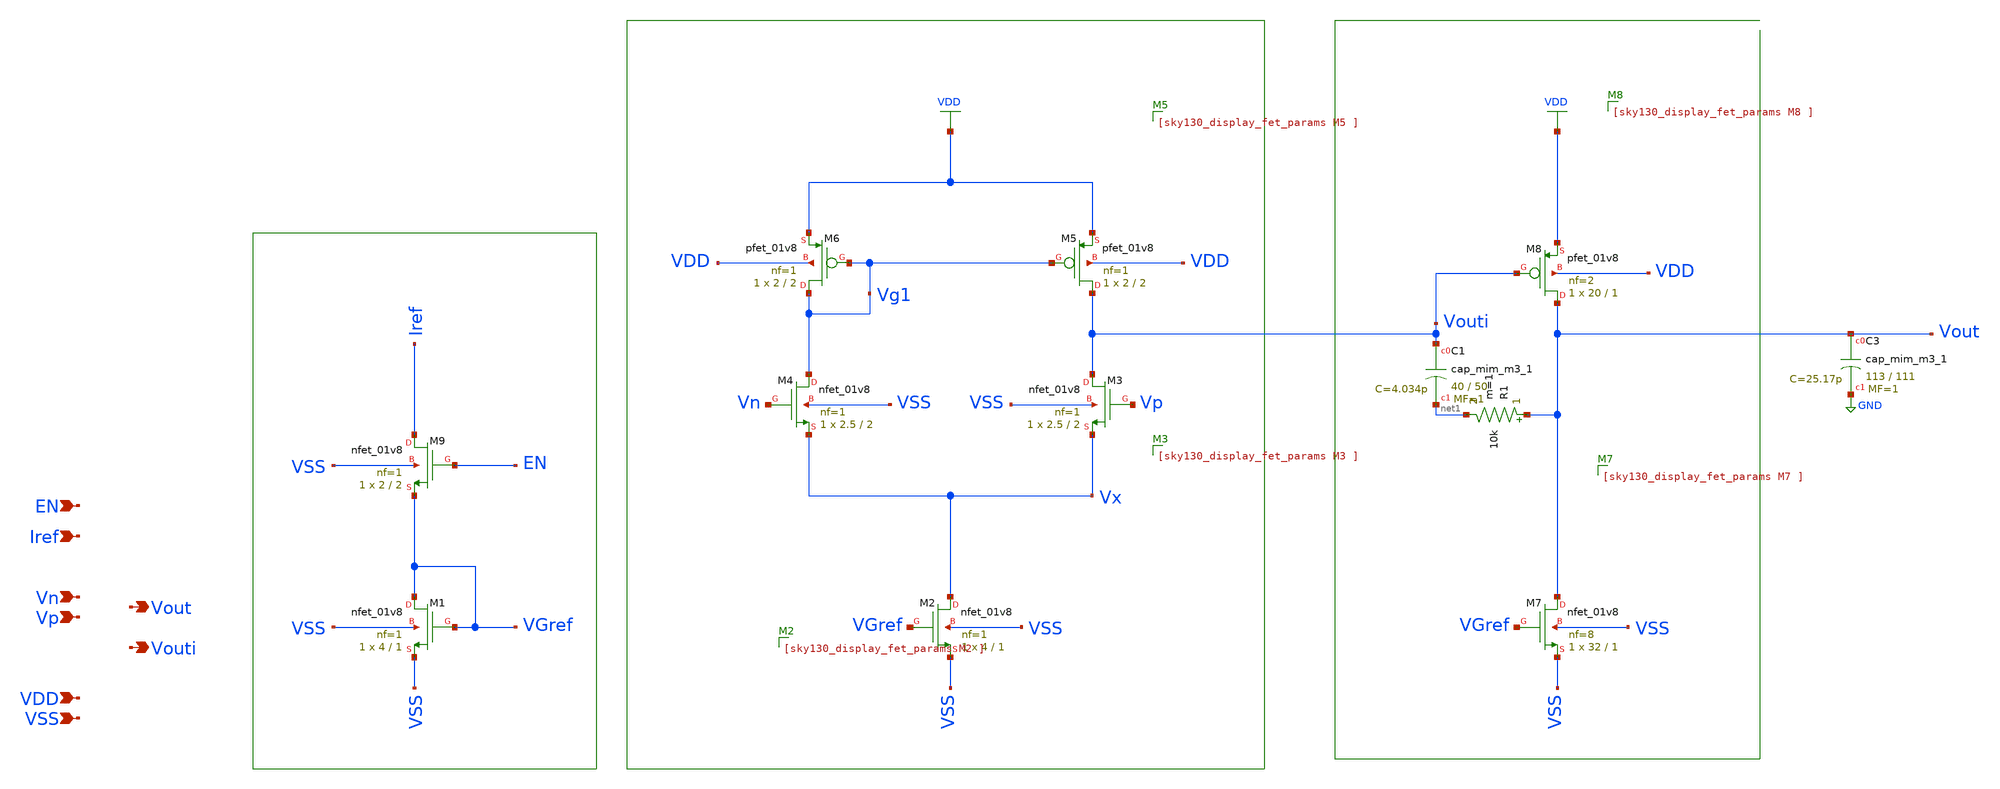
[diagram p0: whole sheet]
** sch_path: xschem/opamp.sch
**.subckt opamp VSS Vp Vout Vn VDD Iref Vouti EN
*.ipin VSS
*.ipin Vp
*.opin Vout
*.ipin Vn
*.ipin VDD
*.ipin Iref
*.opin Vouti
*.ipin EN
XM1 VGref VGref VSS VSS sky130_fd_pr__nfet_01v8 L=1 W=4 nf=1 ad='int((1 + 1)/2) * 4 / 1 * 0.29' as='int((1 + 2)/2) * 4 / 1 * 0.29'
+ pd='2*int((1 + 1)/2) * (4 / 1 + 0.29)' ps='2*int((1 + 2)/2) * (4 / 1 + 0.29)' nrd='0.29 / 4 ' nrs='0.29 / 4 '
+ sa=0 sb=0 sd=0 mult=1 m=1
XM2 Vx VGref VSS VSS sky130_fd_pr__nfet_01v8 L=1 W=4 nf=1 ad='int((1 + 1)/2) * 4 / 1 * 0.29' as='int((1 + 2)/2) * 4 / 1 * 0.29'
+ pd='2*int((1 + 1)/2) * (4 / 1 + 0.29)' ps='2*int((1 + 2)/2) * (4 / 1 + 0.29)' nrd='0.29 / 4 ' nrs='0.29 / 4 '
+ sa=0 sb=0 sd=0 mult=1 m=1
XM3 Vouti Vp Vx VSS sky130_fd_pr__nfet_01v8 L=2 W=2.5 nf=1 ad='int((1 + 1)/2) * 2.5 / 1 * 0.29' as='int((1 + 2)/2) * 2.5 / 1 * 0.29'
+ pd='2*int((1 + 1)/2) * (2.5 / 1 + 0.29)' ps='2*int((1 + 2)/2) * (2.5 / 1 + 0.29)' nrd='0.29 / 2.5 ' nrs='0.29 / 2.5 '
+ sa=0 sb=0 sd=0 mult=1 m=1
XM4 Vg1 Vn Vx VSS sky130_fd_pr__nfet_01v8 L=2 W=2.5 nf=1 ad='int((1 + 1)/2) * 2.5 / 1 * 0.29' as='int((1 + 2)/2) * 2.5 / 1 * 0.29'
+ pd='2*int((1 + 1)/2) * (2.5 / 1 + 0.29)' ps='2*int((1 + 2)/2) * (2.5 / 1 + 0.29)' nrd='0.29 / 2.5 ' nrs='0.29 / 2.5 '
+ sa=0 sb=0 sd=0 mult=1 m=1
XM5 Vouti Vg1 VDD VDD sky130_fd_pr__pfet_01v8 L=2 W=2 nf=1 ad='int((1 + 1)/2) * 2 / 1 * 0.29' as='int((1 + 2)/2) * 2 / 1 * 0.29'
+ pd='2*int((1 + 1)/2) * (2 / 1 + 0.29)' ps='2*int((1 + 2)/2) * (2 / 1 + 0.29)' nrd='0.29 / 2 ' nrs='0.29 / 2 '
+ sa=0 sb=0 sd=0 mult=1 m=1
XM6 Vg1 Vg1 VDD VDD sky130_fd_pr__pfet_01v8 L=2 W=2 nf=1 ad='int((1 + 1)/2) * 2 / 1 * 0.29' as='int((1 + 2)/2) * 2 / 1 * 0.29'
+ pd='2*int((1 + 1)/2) * (2 / 1 + 0.29)' ps='2*int((1 + 2)/2) * (2 / 1 + 0.29)' nrd='0.29 / 2 ' nrs='0.29 / 2 '
+ sa=0 sb=0 sd=0 mult=1 m=1
XM7 Vout VGref VSS VSS sky130_fd_pr__nfet_01v8 L=1 W=32 nf=8 ad='int((8 + 1)/2) * 32 / 8 * 0.29' as='int((8 + 2)/2) * 32 / 8 * 0.29'
+ pd='2*int((8 + 1)/2) * (32 / 8 + 0.29)' ps='2*int((8 + 2)/2) * (32 / 8 + 0.29)' nrd='0.29 / 32 ' nrs='0.29 / 32 '
+ sa=0 sb=0 sd=0 mult=1 m=1
XM8 Vout Vouti VDD VDD sky130_fd_pr__pfet_01v8 L=1 W=20 nf=2 ad='int((2 + 1)/2) * 20 / 2 * 0.29' as='int((2 + 2)/2) * 20 / 2 * 0.29'
+ pd='2*int((2 + 1)/2) * (20 / 2 + 0.29)' ps='2*int((2 + 2)/2) * (20 / 2 + 0.29)' nrd='0.29 / 20 ' nrs='0.29 / 20 '
+ sa=0 sb=0 sd=0 mult=1 m=1
R1 Vout net1 10k m=1
XM9 Iref EN VGref VSS sky130_fd_pr__nfet_01v8 L=2 W=2 nf=1 ad='int((1 + 1)/2) * 2 / 1 * 0.29' as='int((1 + 2)/2) * 2 / 1 * 0.29'
+ pd='2*int((1 + 1)/2) * (2 / 1 + 0.29)' ps='2*int((1 + 2)/2) * (2 / 1 + 0.29)' nrd='0.29 / 2 ' nrs='0.29 / 2 '
+ sa=0 sb=0 sd=0 mult=1 m=1
XC3 Vout GND sky130_fd_pr__cap_mim_m3_1 W=113 L=111 MF=1 m=1
XC1 Vouti net1 sky130_fd_pr__cap_mim_m3_1 W=40 L=50 MF=1 m=1
**.ends
.GLOBAL VDD
.GLOBAL GND
.end
